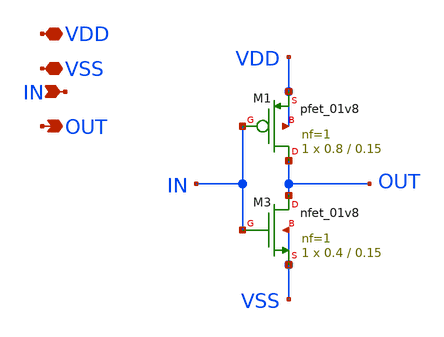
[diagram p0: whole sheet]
** sch_path: Xschem/PLL_TOP/PFD_INV.sch
**.subckt PFD_INV VDD VSS IN OUT
*.iopin VDD
*.iopin VSS
*.ipin IN
*.opin OUT
XM1 OUT IN VDD VDD sky130_fd_pr__pfet_01v8 L=0.15 W=0.8 nf=1 ad='int((nf+1)/2) * W/nf * 0.29' as='int((nf+2)/2) * W/nf * 0.29'
+ pd='2*int((nf+1)/2) * (W/nf + 0.29)' ps='2*int((nf+2)/2) * (W/nf + 0.29)' nrd='0.29 / W' nrs='0.29 / W'
+ sa=0 sb=0 sd=0 mult=1 m=1
XM3 OUT IN VSS VSS sky130_fd_pr__nfet_01v8 L=0.15 W=0.4 nf=1 ad='int((nf+1)/2) * W/nf * 0.29' as='int((nf+2)/2) * W/nf * 0.29'
+ pd='2*int((nf+1)/2) * (W/nf + 0.29)' ps='2*int((nf+2)/2) * (W/nf + 0.29)' nrd='0.29 / W' nrs='0.29 / W'
+ sa=0 sb=0 sd=0 mult=1 m=1
**.ends
.end
